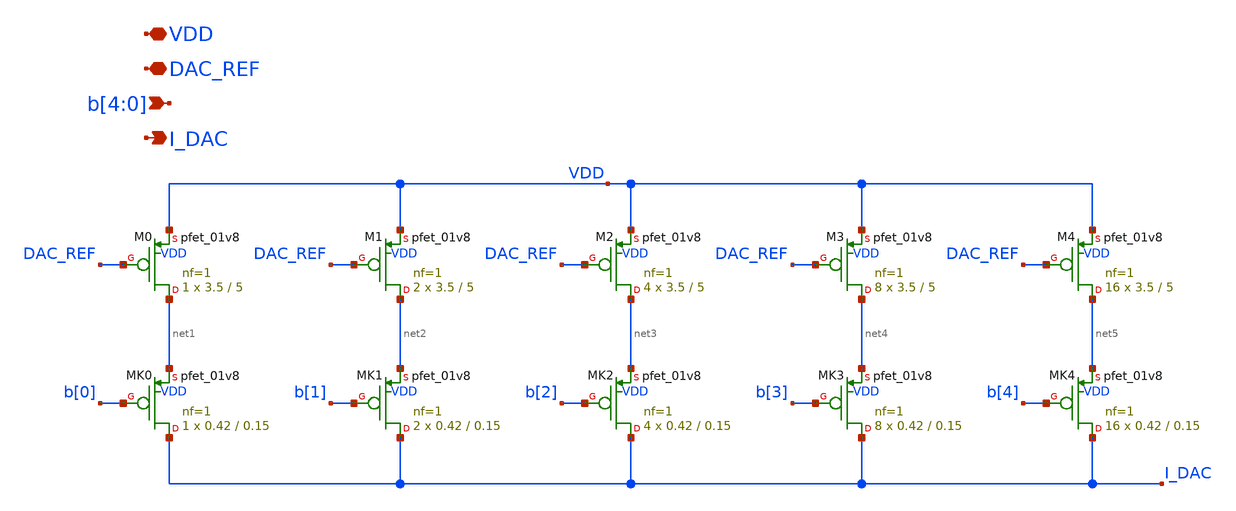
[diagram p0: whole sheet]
** sch_path: designs_backup/designs/lab2/DAC_CORE_5bit.sch
**.subckt DAC_CORE_5bit DAC_REF b[4],b[3],b[2],b[1],b[0] VDD I_DAC
*.iopin DAC_REF
*.ipin b[4],b[3],b[2],b[1],b[0]
*.iopin VDD
*.opin I_DAC
XM1 net2 DAC_REF VDD VDD sky130_fd_pr__pfet_01v8 L=5 W=3.5 nf=1 ad='int((1 + 1)/2) * 3.5 / 1 * 0.29'
+ as='int((1 + 2)/2) * 3.5 / 1 * 0.29' pd='2*int((1 + 1)/2) * (3.5 / 1 + 0.29)' ps='2*int((1 + 2)/2) * (3.5 / 1 + 0.29)'
+ nrd='0.29 / 3.5 ' nrs='0.29 / 3.5 ' sa=0 sb=0 sd=0 mult=2 m=2
XM2 net3 DAC_REF VDD VDD sky130_fd_pr__pfet_01v8 L=5 W=3.5 nf=1 ad='int((1 + 1)/2) * 3.5 / 1 * 0.29'
+ as='int((1 + 2)/2) * 3.5 / 1 * 0.29' pd='2*int((1 + 1)/2) * (3.5 / 1 + 0.29)' ps='2*int((1 + 2)/2) * (3.5 / 1 + 0.29)'
+ nrd='0.29 / 3.5 ' nrs='0.29 / 3.5 ' sa=0 sb=0 sd=0 mult=4 m=4
XM3 net4 DAC_REF VDD VDD sky130_fd_pr__pfet_01v8 L=5 W=3.5 nf=1 ad='int((1 + 1)/2) * 3.5 / 1 * 0.29'
+ as='int((1 + 2)/2) * 3.5 / 1 * 0.29' pd='2*int((1 + 1)/2) * (3.5 / 1 + 0.29)' ps='2*int((1 + 2)/2) * (3.5 / 1 + 0.29)'
+ nrd='0.29 / 3.5 ' nrs='0.29 / 3.5 ' sa=0 sb=0 sd=0 mult=8 m=8
XM4 net5 DAC_REF VDD VDD sky130_fd_pr__pfet_01v8 L=5 W=3.5 nf=1 ad='int((1 + 1)/2) * 3.5 / 1 * 0.29'
+ as='int((1 + 2)/2) * 3.5 / 1 * 0.29' pd='2*int((1 + 1)/2) * (3.5 / 1 + 0.29)' ps='2*int((1 + 2)/2) * (3.5 / 1 + 0.29)'
+ nrd='0.29 / 3.5 ' nrs='0.29 / 3.5 ' sa=0 sb=0 sd=0 mult=16 m=16
XM0 net1 DAC_REF VDD VDD sky130_fd_pr__pfet_01v8 L=5 W=3.5 nf=1 ad='int((1 + 1)/2) * 3.5 / 1 * 0.29'
+ as='int((1 + 2)/2) * 3.5 / 1 * 0.29' pd='2*int((1 + 1)/2) * (3.5 / 1 + 0.29)' ps='2*int((1 + 2)/2) * (3.5 / 1 + 0.29)'
+ nrd='0.29 / 3.5 ' nrs='0.29 / 3.5 ' sa=0 sb=0 sd=0 mult=1 m=1
XMK0 I_DAC b[0] net1 VDD sky130_fd_pr__pfet_01v8 L=0.15 W=0.42 nf=1 ad='int((1 + 1)/2) * 0.42 / 1 * 0.29'
+ as='int((1 + 2)/2) * 0.42 / 1 * 0.29' pd='2*int((1 + 1)/2) * (0.42 / 1 + 0.29)' ps='2*int((1 + 2)/2) * (0.42 / 1 + 0.29)'
+ nrd='0.29 / 0.42 ' nrs='0.29 / 0.42 ' sa=0 sb=0 sd=0 mult=1 m=1
XMK1 I_DAC b[1] net2 VDD sky130_fd_pr__pfet_01v8 L=0.15 W=0.42 nf=1 ad='int((1 + 1)/2) * 0.42 / 1 * 0.29'
+ as='int((1 + 2)/2) * 0.42 / 1 * 0.29' pd='2*int((1 + 1)/2) * (0.42 / 1 + 0.29)' ps='2*int((1 + 2)/2) * (0.42 / 1 + 0.29)'
+ nrd='0.29 / 0.42 ' nrs='0.29 / 0.42 ' sa=0 sb=0 sd=0 mult=2 m=2
XMK2 I_DAC b[2] net3 VDD sky130_fd_pr__pfet_01v8 L=0.15 W=0.42 nf=1 ad='int((1 + 1)/2) * 0.42 / 1 * 0.29'
+ as='int((1 + 2)/2) * 0.42 / 1 * 0.29' pd='2*int((1 + 1)/2) * (0.42 / 1 + 0.29)' ps='2*int((1 + 2)/2) * (0.42 / 1 + 0.29)'
+ nrd='0.29 / 0.42 ' nrs='0.29 / 0.42 ' sa=0 sb=0 sd=0 mult=4 m=4
XMK3 I_DAC b[3] net4 VDD sky130_fd_pr__pfet_01v8 L=0.15 W=0.42 nf=1 ad='int((1 + 1)/2) * 0.42 / 1 * 0.29'
+ as='int((1 + 2)/2) * 0.42 / 1 * 0.29' pd='2*int((1 + 1)/2) * (0.42 / 1 + 0.29)' ps='2*int((1 + 2)/2) * (0.42 / 1 + 0.29)'
+ nrd='0.29 / 0.42 ' nrs='0.29 / 0.42 ' sa=0 sb=0 sd=0 mult=8 m=8
XMK4 I_DAC b[4] net5 VDD sky130_fd_pr__pfet_01v8 L=0.15 W=0.42 nf=1 ad='int((1 + 1)/2) * 0.42 / 1 * 0.29'
+ as='int((1 + 2)/2) * 0.42 / 1 * 0.29' pd='2*int((1 + 1)/2) * (0.42 / 1 + 0.29)' ps='2*int((1 + 2)/2) * (0.42 / 1 + 0.29)'
+ nrd='0.29 / 0.42 ' nrs='0.29 / 0.42 ' sa=0 sb=0 sd=0 mult=16 m=16
**.ends
.end
